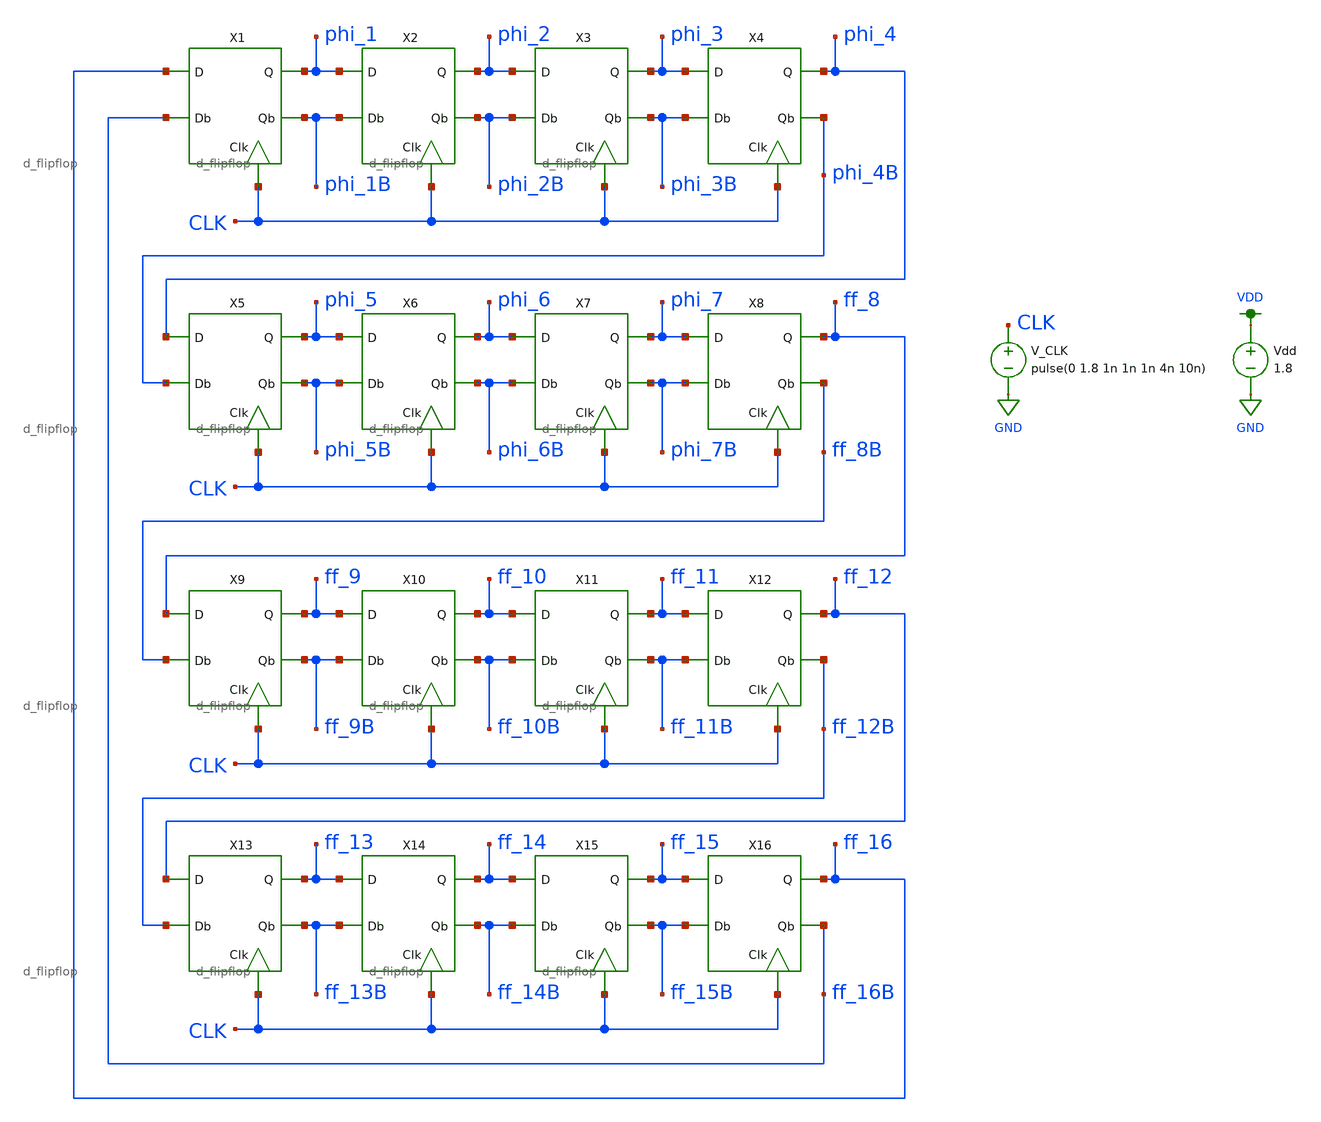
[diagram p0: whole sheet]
** sch_path: simulation/shift_register/shift_register_tran_working.sch
**.subckt shift_register_tran_working
V_CLK CLK GND pulse(0 1.8 1n 1n 1n 4n 10n)
X1 ff_16 ff_16B CLK phi_1B phi_1 d_flipflop
X2 phi_1 phi_1B CLK phi_2B phi_2 d_flipflop
X3 phi_2 phi_2B CLK phi_3B phi_3 d_flipflop
X4 phi_3 phi_3B CLK phi_4B phi_4 d_flipflop
X5 phi_4 phi_4B CLK phi_5B phi_5 d_flipflop
X6 phi_5 phi_5B CLK phi_6B phi_6 d_flipflop
X7 phi_6 phi_6B CLK phi_7B phi_7 d_flipflop
X8 phi_7 phi_7B CLK ff_8B ff_8 d_flipflop
X9 ff_8 ff_8B CLK ff_9B ff_9 d_flipflop
X10 ff_9 ff_9B CLK ff_10B ff_10 d_flipflop
X11 ff_10 ff_10B CLK ff_11B ff_11 d_flipflop
X12 ff_11 ff_11B CLK ff_12B ff_12 d_flipflop
X13 ff_12 ff_12B CLK ff_13B ff_13 d_flipflop
X14 ff_13 ff_13B CLK ff_14B ff_14 d_flipflop
X15 ff_14 ff_14B CLK ff_15B ff_15 d_flipflop
X16 ff_15 ff_15B CLK ff_16B ff_16 d_flipflop
Vdd VDD GND 1.8
**** begin user architecture code

.option wnflag=1
.param MC_SWITCH=0.0
.lib ~/skywater/skywater-pdk/libraries/sky130_fd_pr_ngspice/latest/models/sky130.lib.spice tt


.ic v(phi_1)=0 v(phi_2)=0 v(phi_3)=0 v(phi_4)=0 v(phi_5)=0 v(phi_6)=0 v(phi_7)=0 v(ff_8)=0
+ v(ff_9)=1.8 v(ff_10)=1.8 v(ff_11)=1.8 v(ff_12)=1.8 v(ff_13)=1.8 v(ff_14)=1.8 v(ff_15)=1.8 v(ff_16)=1.8
.tran 0.01n 1u
.save all

**** end user architecture code
**.ends

* expanding   symbol:
*+  /home/madvlsi/Documents/VLSI_Sine_Gen/simulation/shift_register/andrew_mp2_files/d_flipflop/d_flipflop.sym # of pins=5
** sym_path: simulation/shift_register/andrew_mp2_files/d_flipflop/d_flipflop.sym
** sch_path: simulation/shift_register/andrew_mp2_files/d_flipflop/d_flipflop.sch
.subckt d_flipflop D Db CLK Qb Q
*.ipin D
*.ipin CLK
*.opin Q
*.opin Qb
*.ipin Db
XM1 D CLK net2 VP sky130_fd_pr__pfet_01v8 L=0.15 W=1 nf=1 ad='int((nf+1)/2) * W/nf * 0.29' as='int((nf+2)/2) * W/nf * 0.29'
+ pd='2*int((nf+1)/2) * (W/nf + 0.29)' ps='2*int((nf+2)/2) * (W/nf + 0.29)' nrd='0.29 / W' nrs='0.29 / W'
+ sa=0 sb=0 sd=0 mult=1 m=1
XM2 Db CLK net3 VP sky130_fd_pr__pfet_01v8 L=0.15 W=1 nf=1 ad='int((nf+1)/2) * W/nf * 0.29' as='int((nf+2)/2) * W/nf * 0.29'
+ pd='2*int((nf+1)/2) * (W/nf + 0.29)' ps='2*int((nf+2)/2) * (W/nf + 0.29)' nrd='0.29 / W' nrs='0.29 / W'
+ sa=0 sb=0 sd=0 mult=1 m=1
XM3 VDD net2 net3 VP sky130_fd_pr__pfet_01v8 L=0.15 W=1 nf=1 ad='int((nf+1)/2) * W/nf * 0.29' as='int((nf+2)/2) * W/nf * 0.29'
+ pd='2*int((nf+1)/2) * (W/nf + 0.29)' ps='2*int((nf+2)/2) * (W/nf + 0.29)' nrd='0.29 / W' nrs='0.29 / W'
+ sa=0 sb=0 sd=0 mult=1 m=1
XM5 net3 net2 net1 VN sky130_fd_pr__nfet_01v8 L=0.15 W=1 nf=1 ad='int((nf+1)/2) * W/nf * 0.29' as='int((nf+2)/2) * W/nf * 0.29'
+ pd='2*int((nf+1)/2) * (W/nf + 0.29)' ps='2*int((nf+2)/2) * (W/nf + 0.29)' nrd='0.29 / W' nrs='0.29 / W'
+ sa=0 sb=0 sd=0 mult=1 m=1
XM7 net1 CLK GND VN sky130_fd_pr__nfet_01v8 L=0.15 W=4 nf=1 ad='int((nf+1)/2) * W/nf * 0.29' as='int((nf+2)/2) * W/nf * 0.29'
+ pd='2*int((nf+1)/2) * (W/nf + 0.29)' ps='2*int((nf+2)/2) * (W/nf + 0.29)' nrd='0.29 / W' nrs='0.29 / W'
+ sa=0 sb=0 sd=0 mult=1 m=1
XM8 Q CLK net2 VN sky130_fd_pr__nfet_01v8 L=0.15 W=1 nf=1 ad='int((nf+1)/2) * W/nf * 0.29' as='int((nf+2)/2) * W/nf * 0.29'
+ pd='2*int((nf+1)/2) * (W/nf + 0.29)' ps='2*int((nf+2)/2) * (W/nf + 0.29)' nrd='0.29 / W' nrs='0.29 / W'
+ sa=0 sb=0 sd=0 mult=1 m=1
XM9 Qb CLK net3 VN sky130_fd_pr__nfet_01v8 L=0.15 W=1 nf=1 ad='int((nf+1)/2) * W/nf * 0.29' as='int((nf+2)/2) * W/nf * 0.29'
+ pd='2*int((nf+1)/2) * (W/nf + 0.29)' ps='2*int((nf+2)/2) * (W/nf + 0.29)' nrd='0.29 / W' nrs='0.29 / W'
+ sa=0 sb=0 sd=0 mult=1 m=1
XM10 net4 Q Qb VP sky130_fd_pr__pfet_01v8 L=0.15 W=1 nf=1 ad='int((nf+1)/2) * W/nf * 0.29' as='int((nf+2)/2) * W/nf * 0.29'
+ pd='2*int((nf+1)/2) * (W/nf + 0.29)' ps='2*int((nf+2)/2) * (W/nf + 0.29)' nrd='0.29 / W' nrs='0.29 / W'
+ sa=0 sb=0 sd=0 mult=1 m=1
XM11 net4 Qb Q VP sky130_fd_pr__pfet_01v8 L=0.15 W=1 nf=1 ad='int((nf+1)/2) * W/nf * 0.29' as='int((nf+2)/2) * W/nf * 0.29'
+ pd='2*int((nf+1)/2) * (W/nf + 0.29)' ps='2*int((nf+2)/2) * (W/nf + 0.29)' nrd='0.29 / W' nrs='0.29 / W'
+ sa=0 sb=0 sd=0 mult=1 m=1
XM12 VDD CLK net4 VP sky130_fd_pr__pfet_01v8 L=0.15 W=4 nf=1 ad='int((nf+1)/2) * W/nf * 0.29' as='int((nf+2)/2) * W/nf * 0.29'
+ pd='2*int((nf+1)/2) * (W/nf + 0.29)' ps='2*int((nf+2)/2) * (W/nf + 0.29)' nrd='0.29 / W' nrs='0.29 / W'
+ sa=0 sb=0 sd=0 mult=1 m=1
XM13 Qb Q GND VN sky130_fd_pr__nfet_01v8 L=0.15 W=1 nf=1 ad='int((nf+1)/2) * W/nf * 0.29' as='int((nf+2)/2) * W/nf * 0.29'
+ pd='2*int((nf+1)/2) * (W/nf + 0.29)' ps='2*int((nf+2)/2) * (W/nf + 0.29)' nrd='0.29 / W' nrs='0.29 / W'
+ sa=0 sb=0 sd=0 mult=1 m=1
XM14 Q Qb GND VN sky130_fd_pr__nfet_01v8 L=0.15 W=1 nf=1 ad='int((nf+1)/2) * W/nf * 0.29' as='int((nf+2)/2) * W/nf * 0.29'
+ pd='2*int((nf+1)/2) * (W/nf + 0.29)' ps='2*int((nf+2)/2) * (W/nf + 0.29)' nrd='0.29 / W' nrs='0.29 / W'
+ sa=0 sb=0 sd=0 mult=1 m=1
XM4 VDD net3 net2 VP sky130_fd_pr__pfet_01v8 L=0.15 W=1 nf=1 ad='int((nf+1)/2) * W/nf * 0.29' as='int((nf+2)/2) * W/nf * 0.29'
+ pd='2*int((nf+1)/2) * (W/nf + 0.29)' ps='2*int((nf+2)/2) * (W/nf + 0.29)' nrd='0.29 / W' nrs='0.29 / W'
+ sa=0 sb=0 sd=0 mult=1 m=1
XM6 net2 net3 net1 VN sky130_fd_pr__nfet_01v8 L=0.15 W=1 nf=1 ad='int((nf+1)/2) * W/nf * 0.29' as='int((nf+2)/2) * W/nf * 0.29'
+ pd='2*int((nf+1)/2) * (W/nf + 0.29)' ps='2*int((nf+2)/2) * (W/nf + 0.29)' nrd='0.29 / W' nrs='0.29 / W'
+ sa=0 sb=0 sd=0 mult=1 m=1
.ends

.GLOBAL GND
.GLOBAL VDD
.end
